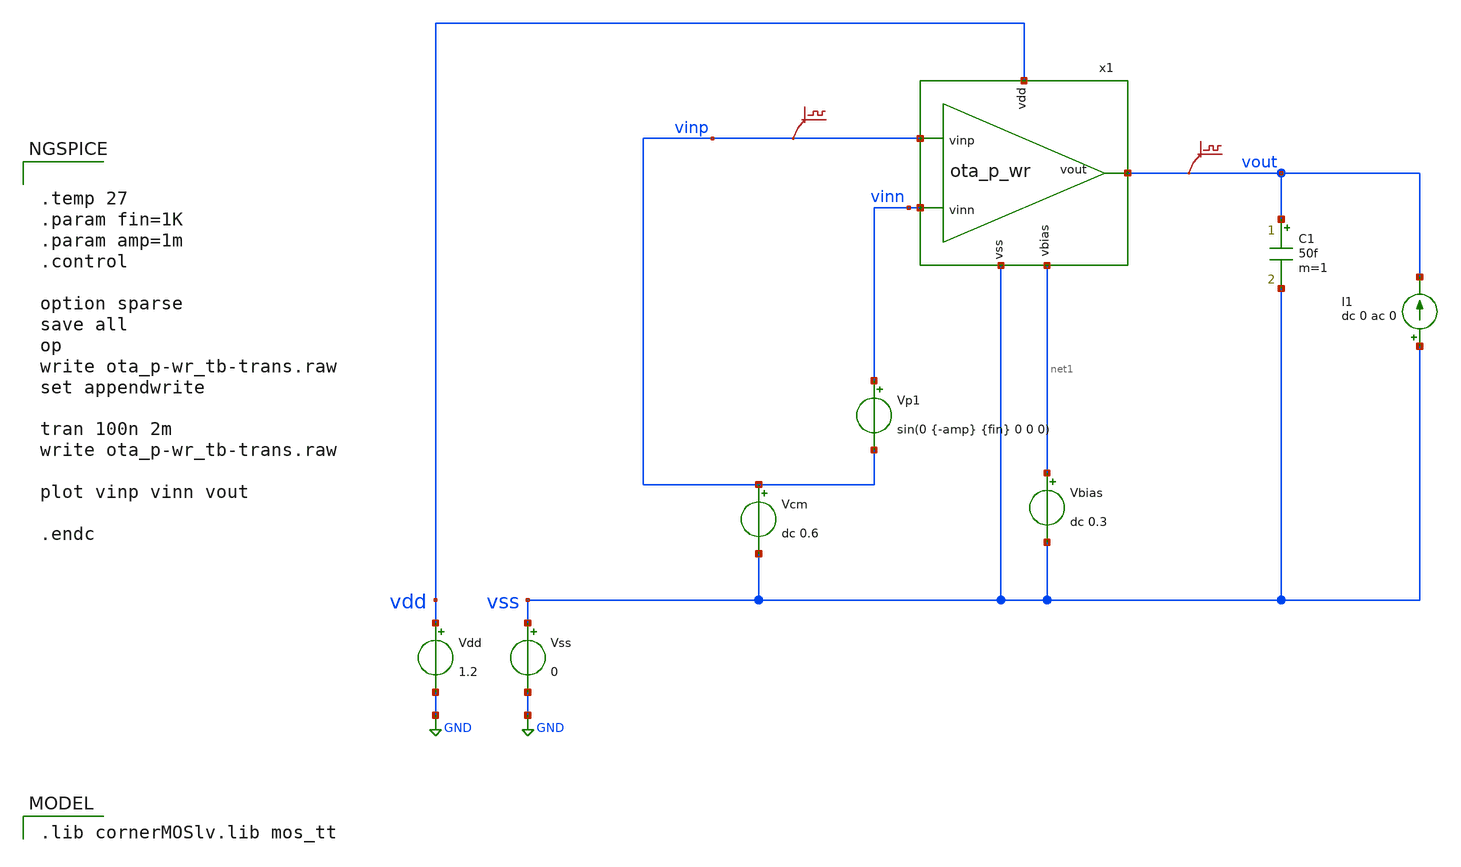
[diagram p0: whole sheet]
** sch_path: v2_feature_extr/ota_p-wr_tb-trans.sch
* (c) 2024-2025 Harald Pretl, Apache-2.0 license
**.subckt ota_p-wr_tb-trans
Vdd vdd GND 1.2
Vss vss GND 0
C1 vout vss 50f m=1
Vcm vinp vss dc 0.6
.save v(vinp)
.save v(vout)
I1 vss vout dc 0 ac 0
Vp1 vinn vinp sin(0 {-amp} {fin} 0 0 0)
Vbias net1 vss dc 0.3
x1 vdd vout vinp vinn net1 vss ota_p_wr
**** begin user architecture code
 .lib cornerMOSlv.lib mos_tt



.temp 27
.param fin=1K
.param amp=1m
.control

option sparse
save all
op
write ota_p-wr_tb-trans.raw
set appendwrite

tran 100n 2m
write ota_p-wr_tb-trans.raw

plot vinp vinn vout

.endc


**** end user architecture code
**.ends
.GLOBAL GND
.end
